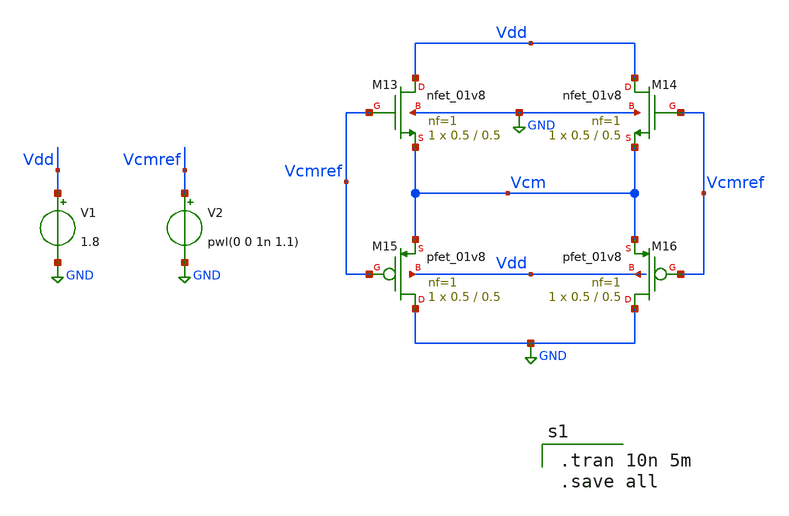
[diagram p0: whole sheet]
** sch_path: xschem/xschemfiles/buffertest.sch
**.subckt buffertest
XM13 Vdd Vcmref Vcm GND sky130_fd_pr__nfet_01v8 L=0.5 W=0.5 nf=1 ad='int((nf+1)/2) * W/nf * 0.29' as='int((nf+2)/2) * W/nf * 0.29'
+ pd='2*int((nf+1)/2) * (W/nf + 0.29)' ps='2*int((nf+2)/2) * (W/nf + 0.29)' nrd='0.29 / W' nrs='0.29 / W'
+ sa=0 sb=0 sd=0 mult=1 m=1
XM14 Vdd Vcmref Vcm GND sky130_fd_pr__nfet_01v8 L=0.5 W=0.5 nf=1 ad='int((nf+1)/2) * W/nf * 0.29' as='int((nf+2)/2) * W/nf * 0.29'
+ pd='2*int((nf+1)/2) * (W/nf + 0.29)' ps='2*int((nf+2)/2) * (W/nf + 0.29)' nrd='0.29 / W' nrs='0.29 / W'
+ sa=0 sb=0 sd=0 mult=1 m=1
XM15 GND Vcmref Vcm Vdd sky130_fd_pr__pfet_01v8 L=0.5 W=0.5 nf=1 ad='int((nf+1)/2) * W/nf * 0.29' as='int((nf+2)/2) * W/nf * 0.29'
+ pd='2*int((nf+1)/2) * (W/nf + 0.29)' ps='2*int((nf+2)/2) * (W/nf + 0.29)' nrd='0.29 / W' nrs='0.29 / W'
+ sa=0 sb=0 sd=0 mult=1 m=1
XM16 GND Vcmref Vcm Vdd sky130_fd_pr__pfet_01v8 L=0.5 W=0.5 nf=1 ad='int((nf+1)/2) * W/nf * 0.29' as='int((nf+2)/2) * W/nf * 0.29'
+ pd='2*int((nf+1)/2) * (W/nf + 0.29)' ps='2*int((nf+2)/2) * (W/nf + 0.29)' nrd='0.29 / W' nrs='0.29 / W'
+ sa=0 sb=0 sd=0 mult=1 m=1
V2 Vcmref GND pwl(0 0 1n 1.1)
V1 Vdd GND 1.8
**** begin user architecture code

.tran 10n 5m
.save all


** opencircuitdesign pdks install
.lib $::SKYWATER_MODELS/sky130.lib.spice tt


**** end user architecture code
**.ends
.GLOBAL GND
.end
